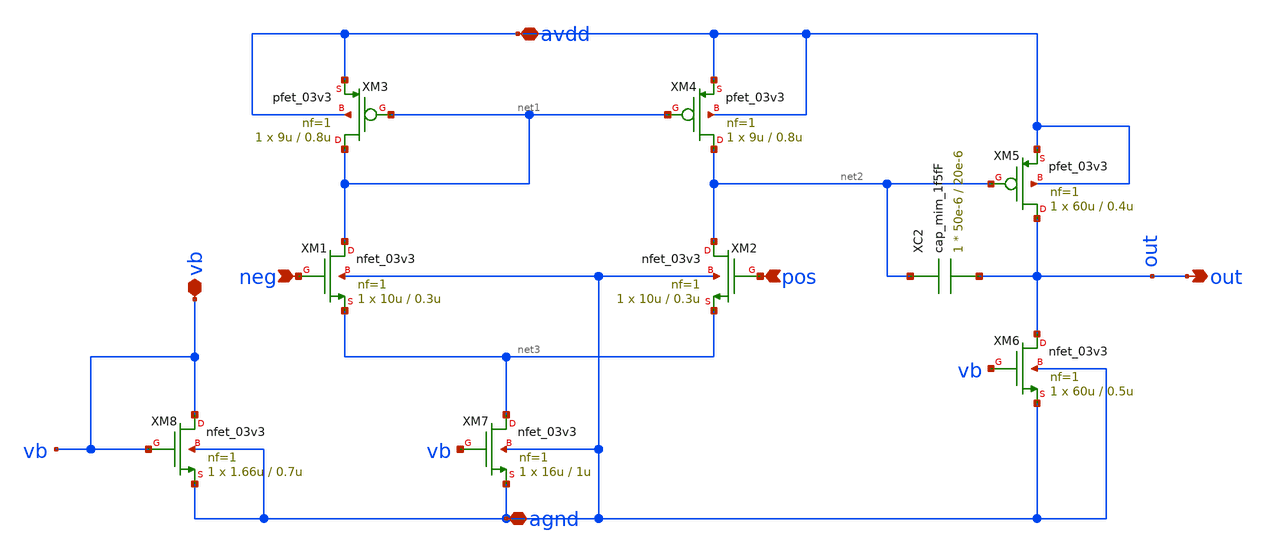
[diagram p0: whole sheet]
** sch_path: LDO/xschem/ota-bandgap/symbol/ota-bandgap.sch
**.subckt ota-bandgap vb avdd agnd neg pos out
*.iopin vb
*.iopin avdd
*.iopin agnd
*.ipin neg
*.ipin pos
*.opin out
XC2 net2 out cap_mim_1f5fF c_width=50e-6 c_length=20e-6 m=1
XM1 net1 neg net3 agnd nfet_03v3 L=0.3u W=10u nf=1 ad='int((nf+1)/2) * W/nf * 0.18u' as='int((nf+2)/2) * W/nf * 0.18u'
+ pd='2*int((nf+1)/2) * (W/nf + 0.18u)' ps='2*int((nf+2)/2) * (W/nf + 0.18u)' nrd='0.18u / W' nrs='0.18u / W'
+ sa=0 sb=0 sd=0 m=1
XM3 net1 net1 avdd avdd pfet_03v3 L=0.8u W=9u nf=1 ad='int((nf+1)/2) * W/nf * 0.18u' as='int((nf+2)/2) * W/nf * 0.18u'
+ pd='2*int((nf+1)/2) * (W/nf + 0.18u)' ps='2*int((nf+2)/2) * (W/nf + 0.18u)' nrd='0.18u / W' nrs='0.18u / W'
+ sa=0 sb=0 sd=0 m=1
XM2 net2 pos net3 agnd nfet_03v3 L=0.3u W=10u nf=1 ad='int((nf+1)/2) * W/nf * 0.18u' as='int((nf+2)/2) * W/nf * 0.18u'
+ pd='2*int((nf+1)/2) * (W/nf + 0.18u)' ps='2*int((nf+2)/2) * (W/nf + 0.18u)' nrd='0.18u / W' nrs='0.18u / W'
+ sa=0 sb=0 sd=0 m=1
XM4 net2 net1 avdd avdd pfet_03v3 L=0.8u W=9u nf=1 ad='int((nf+1)/2) * W/nf * 0.18u' as='int((nf+2)/2) * W/nf * 0.18u'
+ pd='2*int((nf+1)/2) * (W/nf + 0.18u)' ps='2*int((nf+2)/2) * (W/nf + 0.18u)' nrd='0.18u / W' nrs='0.18u / W'
+ sa=0 sb=0 sd=0 m=1
XM7 net3 vb agnd agnd nfet_03v3 L=1u W=16u nf=1 ad='int((nf+1)/2) * W/nf * 0.18u' as='int((nf+2)/2) * W/nf * 0.18u'
+ pd='2*int((nf+1)/2) * (W/nf + 0.18u)' ps='2*int((nf+2)/2) * (W/nf + 0.18u)' nrd='0.18u / W' nrs='0.18u / W'
+ sa=0 sb=0 sd=0 m=1
XM8 vb vb agnd agnd nfet_03v3 L=0.7u W=1.66u nf=1 ad='int((nf+1)/2) * W/nf * 0.18u' as='int((nf+2)/2) * W/nf * 0.18u'
+ pd='2*int((nf+1)/2) * (W/nf + 0.18u)' ps='2*int((nf+2)/2) * (W/nf + 0.18u)' nrd='0.18u / W' nrs='0.18u / W'
+ sa=0 sb=0 sd=0 m=1
XM5 out net2 avdd avdd pfet_03v3 L=0.4u W=60u nf=1 ad='int((nf+1)/2) * W/nf * 0.18u' as='int((nf+2)/2) * W/nf * 0.18u'
+ pd='2*int((nf+1)/2) * (W/nf + 0.18u)' ps='2*int((nf+2)/2) * (W/nf + 0.18u)' nrd='0.18u / W' nrs='0.18u / W'
+ sa=0 sb=0 sd=0 m=1
XM6 out vb agnd agnd nfet_03v3 L=0.5u W=60u nf=1 ad='int((nf+1)/2) * W/nf * 0.18u' as='int((nf+2)/2) * W/nf * 0.18u'
+ pd='2*int((nf+1)/2) * (W/nf + 0.18u)' ps='2*int((nf+2)/2) * (W/nf + 0.18u)' nrd='0.18u / W' nrs='0.18u / W'
+ sa=0 sb=0 sd=0 m=1
**.ends
.end
